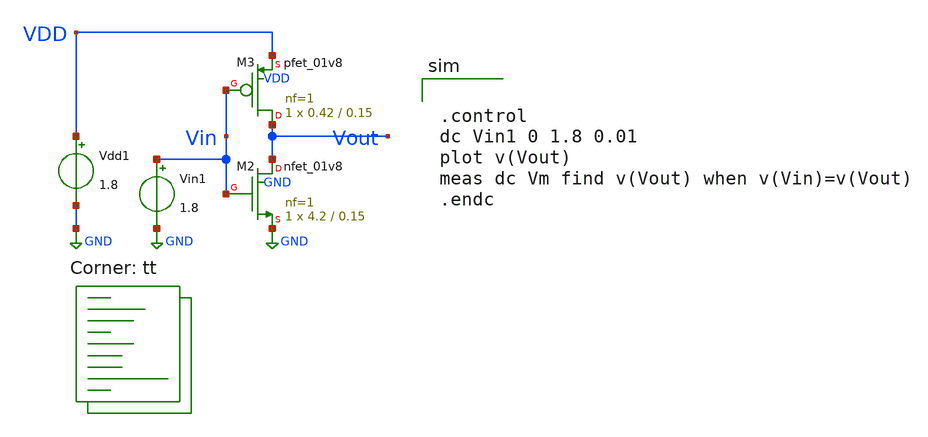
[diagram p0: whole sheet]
** sch_path: tutorial_3/tutorial_3_1b2.sch
**.subckt tutorial_3_1b2
XM2 Vout Vin GND GND sky130_fd_pr__nfet_01v8 L=0.15 W=4.2 nf=1 ad='int((nf+1)/2) * W/nf * 0.29' as='int((nf+2)/2) * W/nf * 0.29'
+ pd='2*int((nf+1)/2) * (W/nf + 0.29)' ps='2*int((nf+2)/2) * (W/nf + 0.29)' nrd='0.29 / W' nrs='0.29 / W'
+ sa=0 sb=0 sd=0 mult=1 m=1
XM3 Vout Vin VDD VDD sky130_fd_pr__pfet_01v8 L=0.15 W=0.42 nf=1 ad='int((nf+1)/2) * W/nf * 0.29' as='int((nf+2)/2) * W/nf * 0.29'
+ pd='2*int((nf+1)/2) * (W/nf + 0.29)' ps='2*int((nf+2)/2) * (W/nf + 0.29)' nrd='0.29 / W' nrs='0.29 / W'
+ sa=0 sb=0 sd=0 mult=1 m=1
Vin1 Vin GND 1.8
Vdd1 VDD GND 1.8
**** begin user architecture code
.lib $::SKYWATER_MODELS/sky130.lib.spice tt


.control
dc Vin1 0 1.8 0.01
plot v(Vout)
meas dc Vm find v(Vout) when v(Vin)=v(Vout)
.endc

**** end user architecture code
**.ends
.GLOBAL GND
.end
